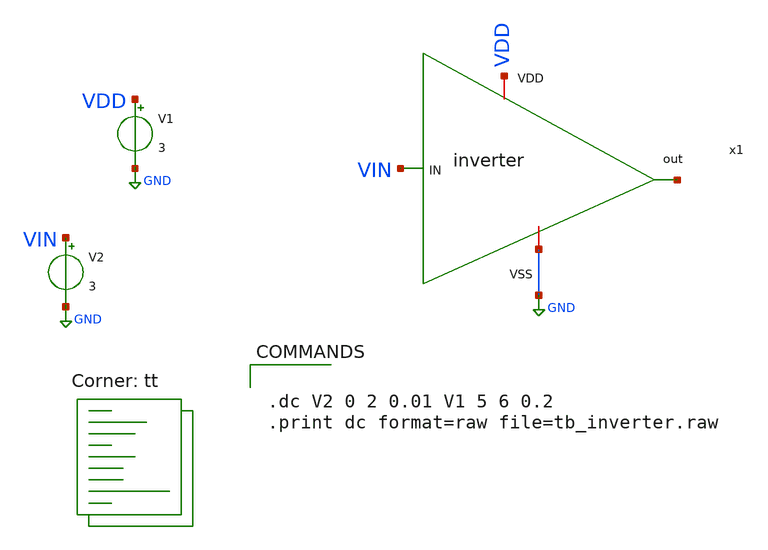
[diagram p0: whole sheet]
** sch_path: tb_inverter.sch
**.subckt tb_inverter
x1 VDD VIN net1 GND inverter
V1 VDD GND 3
V2 VIN GND 3
**** begin user architecture code


.dc V2 0 2 0.01 V1 5 6 0.2
.print dc format=raw file=tb_inverter.raw

.lib $::SKYWATER_MODELS/sky130.lib.spice tt
**** end user architecture code
**.ends

* expanding   symbol:  /home/ttuser/Documents/ADCAnalogDesign/inverter.sym # of pins=4
** sym_path: inverter.sym
** sch_path: inverter.sch
.subckt inverter VDD IN out VSS
*.ipin IN
*.opin out
*.iopin VDD
*.iopin VSS
XM3 out IN VDD VDD sky130_fd_pr__pfet_01v8 L=0.15 W=1 nf=1 ad='int((nf+1)/2) * W/nf * 0.29' as='int((nf+2)/2) * W/nf * 0.29'
+ pd='2*int((nf+1)/2) * (W/nf + 0.29)' ps='2*int((nf+2)/2) * (W/nf + 0.29)' nrd='0.29 / W' nrs='0.29 / W'
+ sa=0 sb=0 sd=0 mult=1 m=1
XM2 out IN VSS VSS sky130_fd_pr__nfet_01v8 L=0.15 W=1 nf=1 ad='int((nf+1)/2) * W/nf * 0.29' as='int((nf+2)/2) * W/nf * 0.29'
+ pd='2*int((nf+1)/2) * (W/nf + 0.29)' ps='2*int((nf+2)/2) * (W/nf + 0.29)' nrd='0.29 / W' nrs='0.29 / W'
+ sa=0 sb=0 sd=0 mult=1 m=1
.ends

.GLOBAL GND
.end
